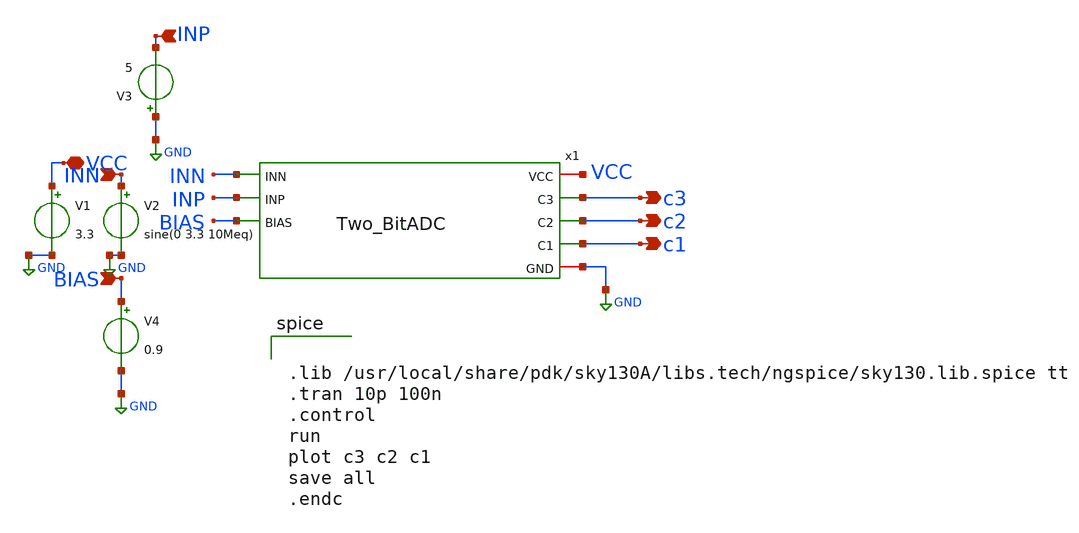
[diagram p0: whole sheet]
** sch_path: week7/pre-layout/tb_2bitADC.sch
**.subckt tb_2bitADC c3 c2 c1 INN BIAS INP VCC
*.opin c3
*.opin c2
*.opin c1
*.ipin INN
*.ipin BIAS
*.ipin INP
*.iopin VCC
x1 INN INP VCC BIAS c3 c2 c1 GND Two_BitADC
V1 VCC GND 3.3
V2 INN GND sine(0 3.3 10Meq)
V3 GND INP 5
V4 BIAS GND 0.9
**** begin user architecture code


.lib /usr/local/share/pdk/sky130A/libs.tech/ngspice/sky130.lib.spice tt
.tran 10p 100n
.control
run
plot c3 c2 c1
save all
.endc

**** end user architecture code
**.ends

* expanding   symbol:  Two_BitADC.sym # of pins=8
** sym_path: week7/pre-layout/Two_BitADC.sym
** sch_path: week7/pre-layout/Two_BitADC.sch
.subckt Two_BitADC INN INP VCC BIAS C3 C2 C1 GND
*.iopin VCC
*.iopin GND
*.ipin BIAS
*.ipin INN
*.ipin INP
*.opin C3
*.opin C2
*.opin C1
x1 VCC C3 INN net1 GND BIAS comp
XR1 net1 INP INP sky130_fd_pr__res_generic_pd W=10 L=5.2 mult=1 m=1
XR2 net2 net1 net1 sky130_fd_pr__res_generic_pd W=10 L=5.2 mult=1 m=1
XR3 net3 net2 net2 sky130_fd_pr__res_generic_pd W=10 L=5.2 mult=1 m=1
XR4 GND net3 net3 sky130_fd_pr__res_generic_pd W=10 L=5.2 mult=1 m=1
x2 VCC C2 INN net2 GND BIAS comp
x3 VCC C1 INN net3 GND BIAS comp
.ends


* expanding   symbol:  comp.sym # of pins=6
** sym_path: week7/pre-layout/comp.sym
** sch_path: week7/pre-layout/comp.sch
.subckt comp VCC OUT INN INP GND BIAS
*.ipin BIAS
*.iopin VCC
*.iopin GND
*.opin OUT
*.ipin INN
*.ipin INP
XM1 net3 net3 VCC VCC sky130_fd_pr__pfet_01v8 L=0.15 W=0.84 nf=1 ad='int((nf+1)/2) * W/nf * 0.29' as='int((nf+2)/2) * W/nf * 0.29'
+ pd='2*int((nf+1)/2) * (W/nf + 0.29)' ps='2*int((nf+2)/2) * (W/nf + 0.29)' nrd='0.29 / W' nrs='0.29 / W'
+ sa=0 sb=0 sd=0 mult=1 m=1
XM3 net3 INN net1 GND sky130_fd_pr__nfet_01v8 L=0.15 W=0.84 nf=1 ad='int((nf+1)/2) * W/nf * 0.29' as='int((nf+2)/2) * W/nf * 0.29'
+ pd='2*int((nf+1)/2) * (W/nf + 0.29)' ps='2*int((nf+2)/2) * (W/nf + 0.29)' nrd='0.29 / W' nrs='0.29 / W'
+ sa=0 sb=0 sd=0 mult=1 m=1
XM12 net1 BIAS GND GND sky130_fd_pr__nfet_01v8 L=0.15 W=0.84 nf=1 ad='int((nf+1)/2) * W/nf * 0.29' as='int((nf+2)/2) * W/nf * 0.29'
+ pd='2*int((nf+1)/2) * (W/nf + 0.29)' ps='2*int((nf+2)/2) * (W/nf + 0.29)' nrd='0.29 / W' nrs='0.29 / W'
+ sa=0 sb=0 sd=0 mult=1 m=1
XM2 net2 net3 VCC VCC sky130_fd_pr__pfet_01v8 L=0.15 W=0.84 nf=1 ad='int((nf+1)/2) * W/nf * 0.29' as='int((nf+2)/2) * W/nf * 0.29'
+ pd='2*int((nf+1)/2) * (W/nf + 0.29)' ps='2*int((nf+2)/2) * (W/nf + 0.29)' nrd='0.29 / W' nrs='0.29 / W'
+ sa=0 sb=0 sd=0 mult=1 m=1
XM4 net2 INP net1 GND sky130_fd_pr__nfet_01v8 L=0.15 W=0.84 nf=1 ad='int((nf+1)/2) * W/nf * 0.29' as='int((nf+2)/2) * W/nf * 0.29'
+ pd='2*int((nf+1)/2) * (W/nf + 0.29)' ps='2*int((nf+2)/2) * (W/nf + 0.29)' nrd='0.29 / W' nrs='0.29 / W'
+ sa=0 sb=0 sd=0 mult=1 m=1
XM5 net4 net2 VCC VCC sky130_fd_pr__pfet_01v8 L=0.15 W=0.84 nf=1 ad='int((nf+1)/2) * W/nf * 0.29' as='int((nf+2)/2) * W/nf * 0.29'
+ pd='2*int((nf+1)/2) * (W/nf + 0.29)' ps='2*int((nf+2)/2) * (W/nf + 0.29)' nrd='0.29 / W' nrs='0.29 / W'
+ sa=0 sb=0 sd=0 mult=1 m=1
XM6 net4 net2 GND GND sky130_fd_pr__nfet_01v8 L=0.15 W=0.84 nf=1 ad='int((nf+1)/2) * W/nf * 0.29' as='int((nf+2)/2) * W/nf * 0.29'
+ pd='2*int((nf+1)/2) * (W/nf + 0.29)' ps='2*int((nf+2)/2) * (W/nf + 0.29)' nrd='0.29 / W' nrs='0.29 / W'
+ sa=0 sb=0 sd=0 mult=1 m=1
XM7 net5 net4 GND GND sky130_fd_pr__nfet_01v8 L=0.15 W=0.84 nf=1 ad='int((nf+1)/2) * W/nf * 0.29' as='int((nf+2)/2) * W/nf * 0.29'
+ pd='2*int((nf+1)/2) * (W/nf + 0.29)' ps='2*int((nf+2)/2) * (W/nf + 0.29)' nrd='0.29 / W' nrs='0.29 / W'
+ sa=0 sb=0 sd=0 mult=1 m=1
XM8 OUT net5 GND GND sky130_fd_pr__nfet_01v8 L=0.15 W=0.84 nf=1 ad='int((nf+1)/2) * W/nf * 0.29' as='int((nf+2)/2) * W/nf * 0.29'
+ pd='2*int((nf+1)/2) * (W/nf + 0.29)' ps='2*int((nf+2)/2) * (W/nf + 0.29)' nrd='0.29 / W' nrs='0.29 / W'
+ sa=0 sb=0 sd=0 mult=1 m=1
XM9 net5 net4 VCC VCC sky130_fd_pr__pfet_01v8 L=0.15 W=0.84 nf=1 ad='int((nf+1)/2) * W/nf * 0.29' as='int((nf+2)/2) * W/nf * 0.29'
+ pd='2*int((nf+1)/2) * (W/nf + 0.29)' ps='2*int((nf+2)/2) * (W/nf + 0.29)' nrd='0.29 / W' nrs='0.29 / W'
+ sa=0 sb=0 sd=0 mult=1 m=1
XM10 OUT net5 VCC VCC sky130_fd_pr__pfet_01v8 L=0.15 W=0.84 nf=1 ad='int((nf+1)/2) * W/nf * 0.29' as='int((nf+2)/2) * W/nf * 0.29'
+ pd='2*int((nf+1)/2) * (W/nf + 0.29)' ps='2*int((nf+2)/2) * (W/nf + 0.29)' nrd='0.29 / W' nrs='0.29 / W'
+ sa=0 sb=0 sd=0 mult=1 m=1
.ends

.GLOBAL GND
.end
